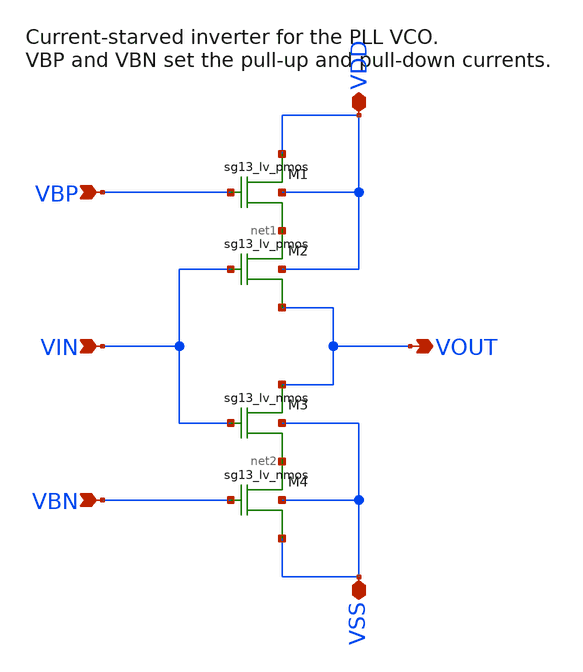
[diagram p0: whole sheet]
** sch_path: schematic/xschem/pll/inverter.sch
**.subckt inverter VIN VBP VBN VOUT VDD VSS
*.ipin VIN
*.ipin VBP
*.ipin VBN
*.opin VOUT
*.iopin VDD
*.iopin VSS
XM1 VDD VBP net1 VDD sg13_lv_pmos w=0.15u l=0.13u ng=1 m=1
XM2 net1 VIN VOUT VDD sg13_lv_pmos w=0.15u l=0.13u ng=1 m=1
XM3 VOUT VIN net2 VSS sg13_lv_nmos w=0.15u l=0.13u ng=1 m=1
XM4 net2 VBN VSS VSS sg13_lv_nmos w=0.15u l=0.13u ng=1 m=1
**.ends
.end
